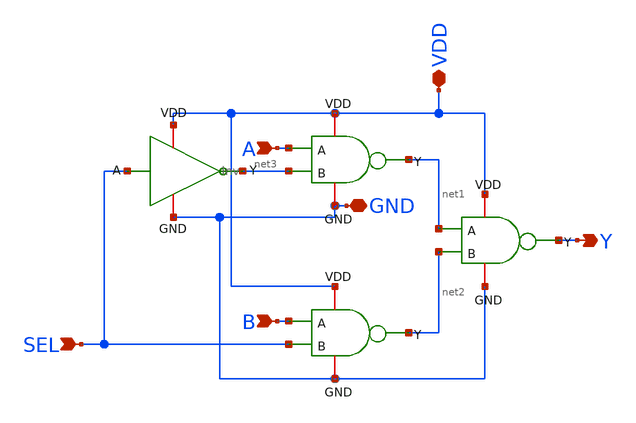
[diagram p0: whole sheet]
** sch_path: Mux2.sch
**.subckt Mux2 A B SEL GND Y VDD
*.ipin A
*.ipin B
*.ipin SEL
*.iopin GND
*.opin Y
*.iopin VDD
x2 VDD net1 net3 A GND NAND
x4 VDD Y net2 net1 GND NAND
x3 VDD net2 SEL B GND NAND
x1 VDD SEL net3 GND Inv
**.ends
.end
